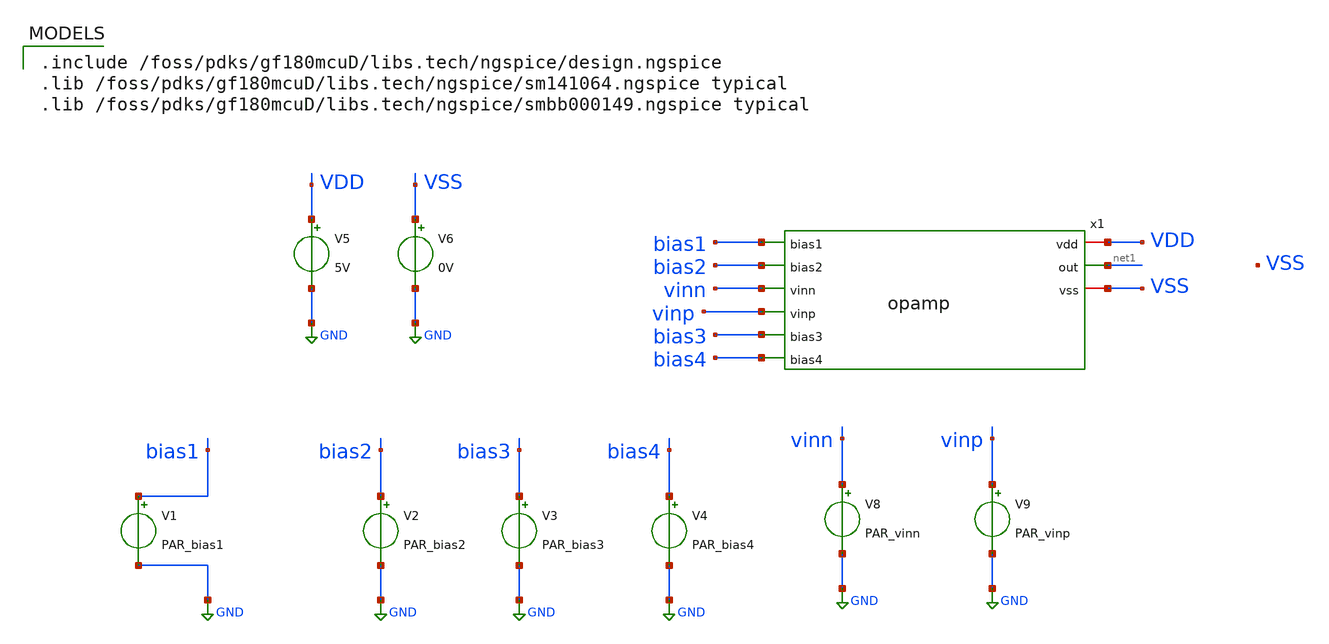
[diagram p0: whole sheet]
** sch_path: activities/opamp2AKAM/testBenchOpamp.sch
**.subckt testBenchOpamp
V1 bias1 GND PAR_bias1
V2 bias2 GND PAR_bias2
V3 bias3 GND PAR_bias3
V4 bias4 GND PAR_bias4
V5 VDD GND 5V
V6 VSS GND 0V
V8 vinn GND PAR_vinn
V9 vinp GND PAR_vinp
x1 VDD bias1 bias2 vinn net1 vinp bias3 bias4 VSS opamp
**** begin user architecture code

.include /foss/pdks/gf180mcuD/libs.tech/ngspice/design.ngspice
.lib /foss/pdks/gf180mcuD/libs.tech/ngspice/sm141064.ngspice typical
.lib /foss/pdks/gf180mcuD/libs.tech/ngspice/smbb000149.ngspice typical

**** end user architecture code
**.ends
.GLOBAL GND
.end
